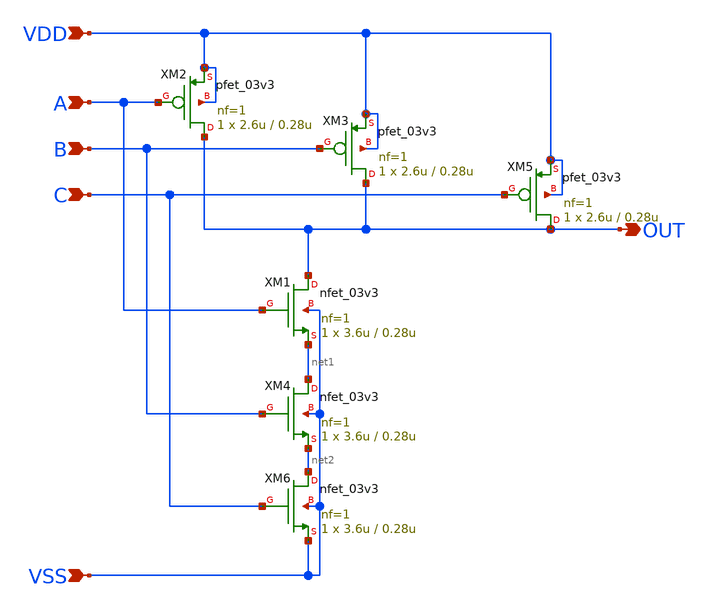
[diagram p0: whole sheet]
** sch_path: Project/1-on-chip/schematic/PNgen/nand_3_out.sch
**.subckt nand_3_out VDD OUT A B VSS C
*.ipin VDD
*.opin OUT
*.ipin A
*.ipin B
*.ipin VSS
*.ipin C
XM1 OUT A net1 VSS nfet_03v3 L=0.28u W=3.6u nf=1 ad='int((nf+1)/2) * W/nf * 0.18u' as='int((nf+2)/2) * W/nf * 0.18u'
+ pd='2*int((nf+1)/2) * (W/nf + 0.18u)' ps='2*int((nf+2)/2) * (W/nf + 0.18u)' nrd='0.18u / W' nrs='0.18u / W'
+ sa=0 sb=0 sd=0 m=1
XM2 OUT A VDD VDD pfet_03v3 L=0.28u W=2.6u nf=1 ad='int((nf+1)/2) * W/nf * 0.18u' as='int((nf+2)/2) * W/nf * 0.18u'
+ pd='2*int((nf+1)/2) * (W/nf + 0.18u)' ps='2*int((nf+2)/2) * (W/nf + 0.18u)' nrd='0.18u / W' nrs='0.18u / W'
+ sa=0 sb=0 sd=0 m=1
XM3 OUT B VDD VDD pfet_03v3 L=0.28u W=2.6u nf=1 ad='int((nf+1)/2) * W/nf * 0.18u' as='int((nf+2)/2) * W/nf * 0.18u'
+ pd='2*int((nf+1)/2) * (W/nf + 0.18u)' ps='2*int((nf+2)/2) * (W/nf + 0.18u)' nrd='0.18u / W' nrs='0.18u / W'
+ sa=0 sb=0 sd=0 m=1
XM4 net1 B net2 VSS nfet_03v3 L=0.28u W=3.6u nf=1 ad='int((nf+1)/2) * W/nf * 0.18u' as='int((nf+2)/2) * W/nf * 0.18u'
+ pd='2*int((nf+1)/2) * (W/nf + 0.18u)' ps='2*int((nf+2)/2) * (W/nf + 0.18u)' nrd='0.18u / W' nrs='0.18u / W'
+ sa=0 sb=0 sd=0 m=1
XM5 OUT C VDD VDD pfet_03v3 L=0.28u W=2.6u nf=1 ad='int((nf+1)/2) * W/nf * 0.18u' as='int((nf+2)/2) * W/nf * 0.18u'
+ pd='2*int((nf+1)/2) * (W/nf + 0.18u)' ps='2*int((nf+2)/2) * (W/nf + 0.18u)' nrd='0.18u / W' nrs='0.18u / W'
+ sa=0 sb=0 sd=0 m=1
XM6 net2 C VSS VSS nfet_03v3 L=0.28u W=3.6u nf=1 ad='int((nf+1)/2) * W/nf * 0.18u' as='int((nf+2)/2) * W/nf * 0.18u'
+ pd='2*int((nf+1)/2) * (W/nf + 0.18u)' ps='2*int((nf+2)/2) * (W/nf + 0.18u)' nrd='0.18u / W' nrs='0.18u / W'
+ sa=0 sb=0 sd=0 m=1
**.ends
.end
